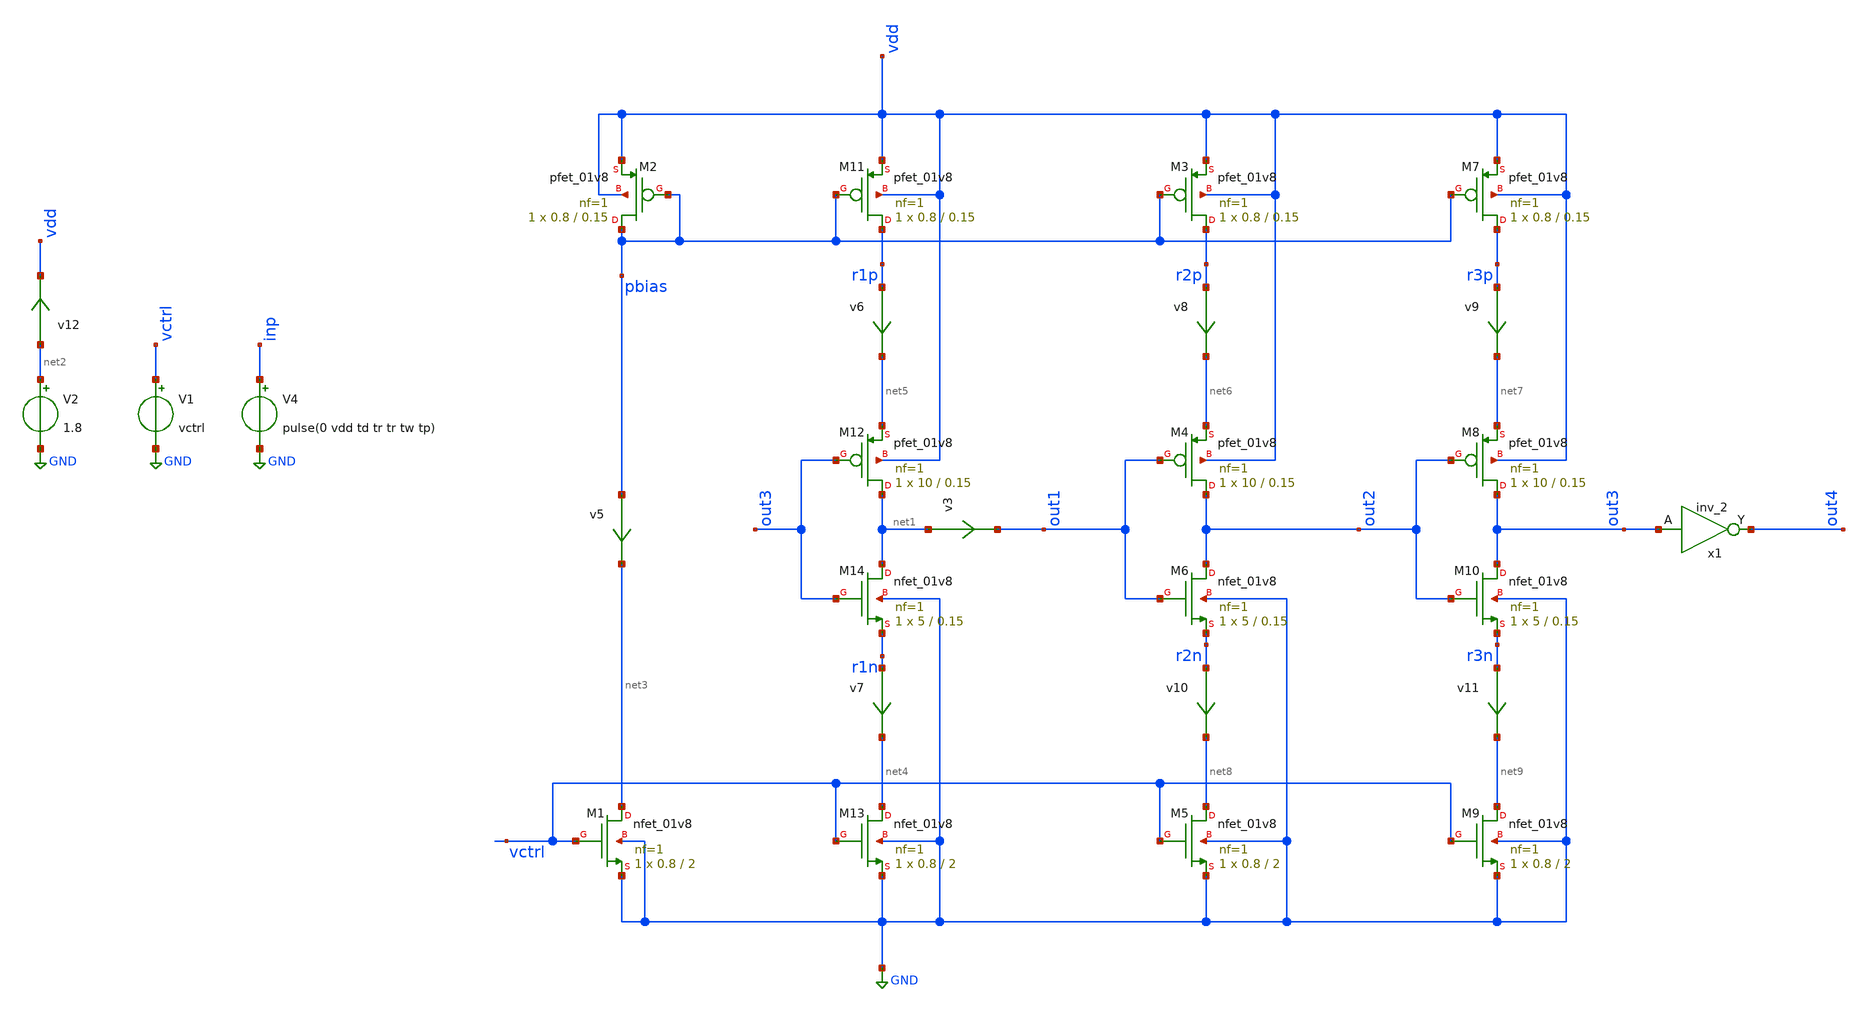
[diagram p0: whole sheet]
** sch_path: xschem/vco/inv_delay.sch
**.subckt inv_delay
XM1 net3 vctrl GND GND sky130_fd_pr__nfet_01v8 L=2 W=0.8 nf=1 ad='int((nf+1)/2) * W/nf * 0.29' as='int((nf+2)/2) * W/nf * 0.29'
+ pd='2*int((nf+1)/2) * (W/nf + 0.29)' ps='2*int((nf+2)/2) * (W/nf + 0.29)' nrd='0.29 / W' nrs='0.29 / W'
+ sa=0 sb=0 sd=0 mult=1 m=1
XM2 pbias pbias vdd vdd sky130_fd_pr__pfet_01v8 L=0.15 W=0.8 nf=1 ad='int((nf+1)/2) * W/nf * 0.29' as='int((nf+2)/2) * W/nf * 0.29'
+ pd='2*int((nf+1)/2) * (W/nf + 0.29)' ps='2*int((nf+2)/2) * (W/nf + 0.29)' nrd='0.29 / W' nrs='0.29 / W'
+ sa=0 sb=0 sd=0 mult=1 m=1
XM11 r1p pbias vdd vdd sky130_fd_pr__pfet_01v8 L=0.15 W=0.8 nf=1 ad='int((nf+1)/2) * W/nf * 0.29' as='int((nf+2)/2) * W/nf * 0.29'
+ pd='2*int((nf+1)/2) * (W/nf + 0.29)' ps='2*int((nf+2)/2) * (W/nf + 0.29)' nrd='0.29 / W' nrs='0.29 / W'
+ sa=0 sb=0 sd=0 mult=1 m=1
XM12 net1 out3 net5 vdd sky130_fd_pr__pfet_01v8 L=0.15 W=10 nf=1 ad='int((nf+1)/2) * W/nf * 0.29' as='int((nf+2)/2) * W/nf * 0.29'
+ pd='2*int((nf+1)/2) * (W/nf + 0.29)' ps='2*int((nf+2)/2) * (W/nf + 0.29)' nrd='0.29 / W' nrs='0.29 / W'
+ sa=0 sb=0 sd=0 mult=1 m=1
XM13 net4 vctrl GND GND sky130_fd_pr__nfet_01v8 L=2 W=0.8 nf=1 ad='int((nf+1)/2) * W/nf * 0.29' as='int((nf+2)/2) * W/nf * 0.29'
+ pd='2*int((nf+1)/2) * (W/nf + 0.29)' ps='2*int((nf+2)/2) * (W/nf + 0.29)' nrd='0.29 / W' nrs='0.29 / W'
+ sa=0 sb=0 sd=0 mult=1 m=1
XM14 net1 out3 r1n GND sky130_fd_pr__nfet_01v8 L=0.15 W=5 nf=1 ad='int((nf+1)/2) * W/nf * 0.29' as='int((nf+2)/2) * W/nf * 0.29'
+ pd='2*int((nf+1)/2) * (W/nf + 0.29)' ps='2*int((nf+2)/2) * (W/nf + 0.29)' nrd='0.29 / W' nrs='0.29 / W'
+ sa=0 sb=0 sd=0 mult=1 m=1
V1 vctrl GND vctrl
V2 net2 GND 1.8
V4 inp GND pulse(0 vdd td tr tr tw tp)
x1 out3 GND GND VDD VDD out4 sky130_fd_sc_hd__inv_2
v3 net1 out1 0
.save i(v3)
v5 pbias net3 0
.save i(v5)
XM3 r2p pbias vdd vdd sky130_fd_pr__pfet_01v8 L=0.15 W=0.8 nf=1 ad='int((nf+1)/2) * W/nf * 0.29' as='int((nf+2)/2) * W/nf * 0.29'
+ pd='2*int((nf+1)/2) * (W/nf + 0.29)' ps='2*int((nf+2)/2) * (W/nf + 0.29)' nrd='0.29 / W' nrs='0.29 / W'
+ sa=0 sb=0 sd=0 mult=1 m=1
XM4 out2 out1 net6 vdd sky130_fd_pr__pfet_01v8 L=0.15 W=10 nf=1 ad='int((nf+1)/2) * W/nf * 0.29' as='int((nf+2)/2) * W/nf * 0.29'
+ pd='2*int((nf+1)/2) * (W/nf + 0.29)' ps='2*int((nf+2)/2) * (W/nf + 0.29)' nrd='0.29 / W' nrs='0.29 / W'
+ sa=0 sb=0 sd=0 mult=1 m=1
XM5 net8 vctrl GND GND sky130_fd_pr__nfet_01v8 L=2 W=0.8 nf=1 ad='int((nf+1)/2) * W/nf * 0.29' as='int((nf+2)/2) * W/nf * 0.29'
+ pd='2*int((nf+1)/2) * (W/nf + 0.29)' ps='2*int((nf+2)/2) * (W/nf + 0.29)' nrd='0.29 / W' nrs='0.29 / W'
+ sa=0 sb=0 sd=0 mult=1 m=1
XM6 out2 out1 r2n GND sky130_fd_pr__nfet_01v8 L=0.15 W=5 nf=1 ad='int((nf+1)/2) * W/nf * 0.29' as='int((nf+2)/2) * W/nf * 0.29'
+ pd='2*int((nf+1)/2) * (W/nf + 0.29)' ps='2*int((nf+2)/2) * (W/nf + 0.29)' nrd='0.29 / W' nrs='0.29 / W'
+ sa=0 sb=0 sd=0 mult=1 m=1
XM7 r3p pbias vdd vdd sky130_fd_pr__pfet_01v8 L=0.15 W=0.8 nf=1 ad='int((nf+1)/2) * W/nf * 0.29' as='int((nf+2)/2) * W/nf * 0.29'
+ pd='2*int((nf+1)/2) * (W/nf + 0.29)' ps='2*int((nf+2)/2) * (W/nf + 0.29)' nrd='0.29 / W' nrs='0.29 / W'
+ sa=0 sb=0 sd=0 mult=1 m=1
XM8 out3 out2 net7 vdd sky130_fd_pr__pfet_01v8 L=0.15 W=10 nf=1 ad='int((nf+1)/2) * W/nf * 0.29' as='int((nf+2)/2) * W/nf * 0.29'
+ pd='2*int((nf+1)/2) * (W/nf + 0.29)' ps='2*int((nf+2)/2) * (W/nf + 0.29)' nrd='0.29 / W' nrs='0.29 / W'
+ sa=0 sb=0 sd=0 mult=1 m=1
XM9 net9 vctrl GND GND sky130_fd_pr__nfet_01v8 L=2 W=0.8 nf=1 ad='int((nf+1)/2) * W/nf * 0.29' as='int((nf+2)/2) * W/nf * 0.29'
+ pd='2*int((nf+1)/2) * (W/nf + 0.29)' ps='2*int((nf+2)/2) * (W/nf + 0.29)' nrd='0.29 / W' nrs='0.29 / W'
+ sa=0 sb=0 sd=0 mult=1 m=1
XM10 out3 out2 r3n GND sky130_fd_pr__nfet_01v8 L=0.15 W=5 nf=1 ad='int((nf+1)/2) * W/nf * 0.29' as='int((nf+2)/2) * W/nf * 0.29'
+ pd='2*int((nf+1)/2) * (W/nf + 0.29)' ps='2*int((nf+2)/2) * (W/nf + 0.29)' nrd='0.29 / W' nrs='0.29 / W'
+ sa=0 sb=0 sd=0 mult=1 m=1
v6 r1p net5 0
.save i(v6)
v7 r1n net4 0
.save i(v7)
v8 r2p net6 0
.save i(v8)
v9 r3p net7 0
.save i(v9)
v10 r2n net8 0
.save i(v10)
v11 r3n net9 0
.save i(v11)
v12 net2 vdd 0
.save i(v12)
**** begin user architecture code

** opencircuitdesign pdks install
.lib $::SKYWATER_MODELS/sky130.lib.spice tt
.include $::SKYWATER_STDCELLS/sky130_fd_sc_hd.spice




.options acct list
.temp 25
.save all
.save @m.xm1.msky130_fd_pr__nfet_01v8[cgd]

.save @m.xm1.msky130_fd_pr__nfet_01v8[ids]

.save @m.xm4.msky130_fd_pr__pfet_01v8[cgd]
.save @m.xm4.msky130_fd_pr__pfet_01v8[cgg]

.save @m.xm6.msky130_fd_pr__nfet_01v8[cgd]
.save @m.xm6.msky130_fd_pr__nfet_01v8[cgg]

.save @m.xm1.msky130_fd_pr__nfet_01v8[gm]
.save @m.xm12.msky130_fd_pr__pfet_01v8[id]
.save @m.xm14.msky130_fd_pr__nfet_01v8[id]

.save @m.xm6.msky130_fd_pr__nfet_01v8[id]
.save @m.xm2.msky130_fd_pr__pfet_01v8[vth]
.save @m.xm1.msky130_fd_pr__nfet_01v8[vth]
.save @m.xm5.msky130_fd_pr__nfet_01v8[vth]



.param vctrl=1.29 vdd=1.8 cload=250f  td=20n tr=0.1n tw=10n  tp=20n

.control
op
write inv_delay.raw
set appendwrite

tran 0.01n 800n uic
meas tran tdelay01 TRIG v(out4) VAL=0.9 RISE=4 TARG v(out4) VAL=0.9 RISE=5
let fosc1= 1/tdelay01
print fosc1
save fosc1
remzerovec
write inv_delay.raw

.endc


**** end user architecture code
**.ends
.GLOBAL GND
.end
